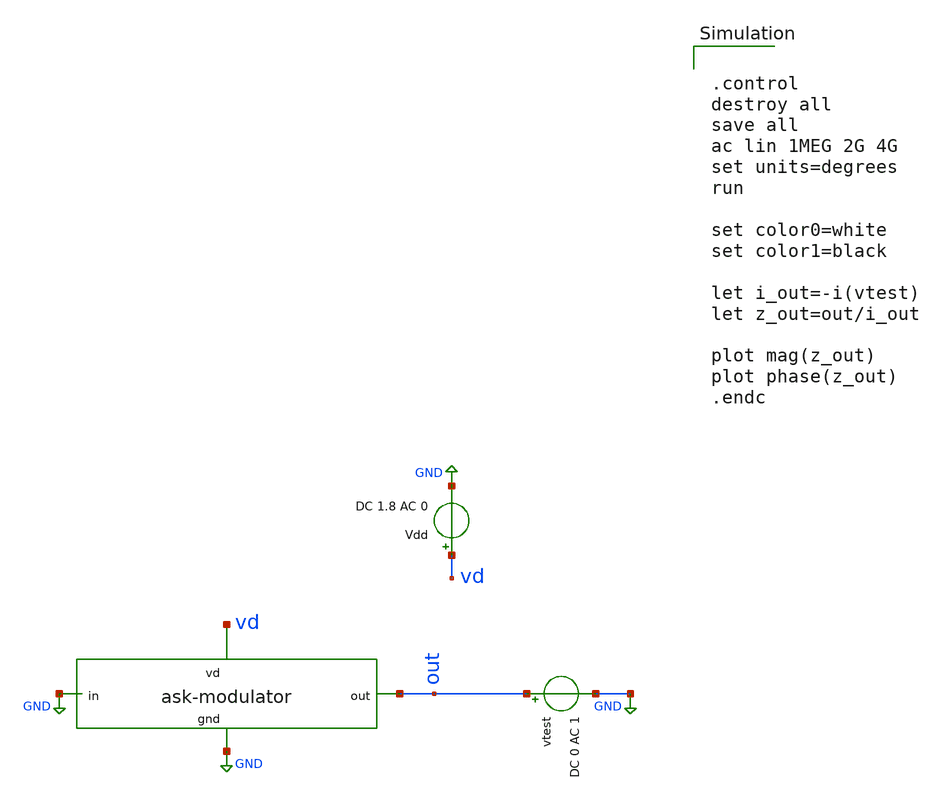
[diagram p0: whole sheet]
** sch_path: ask_modulator/xschem/ask-modulator_tb-ac.sch
**.subckt ask-modulator_tb-ac
Vdd vd GND DC 1.8 AC 0
vtest out GND DC 0 AC 1
xask1 vd out GND GND ask-modulator
**** begin user architecture code


.control
destroy all
save all
ac lin 1MEG 2G 4G
set units=degrees
run

set color0=white
set color1=black

let i_out=-i(vtest)
let z_out=out/i_out

plot mag(z_out)
plot phase(z_out)
.endc

 .lib $::SKYWATER_MODELS/sky130.lib.spice tt
.include $::SKYWATER_STDCELLS/sky130_fd_sc_hd.spice

**** end user architecture code
**.ends
.GLOBAL GND
.end
